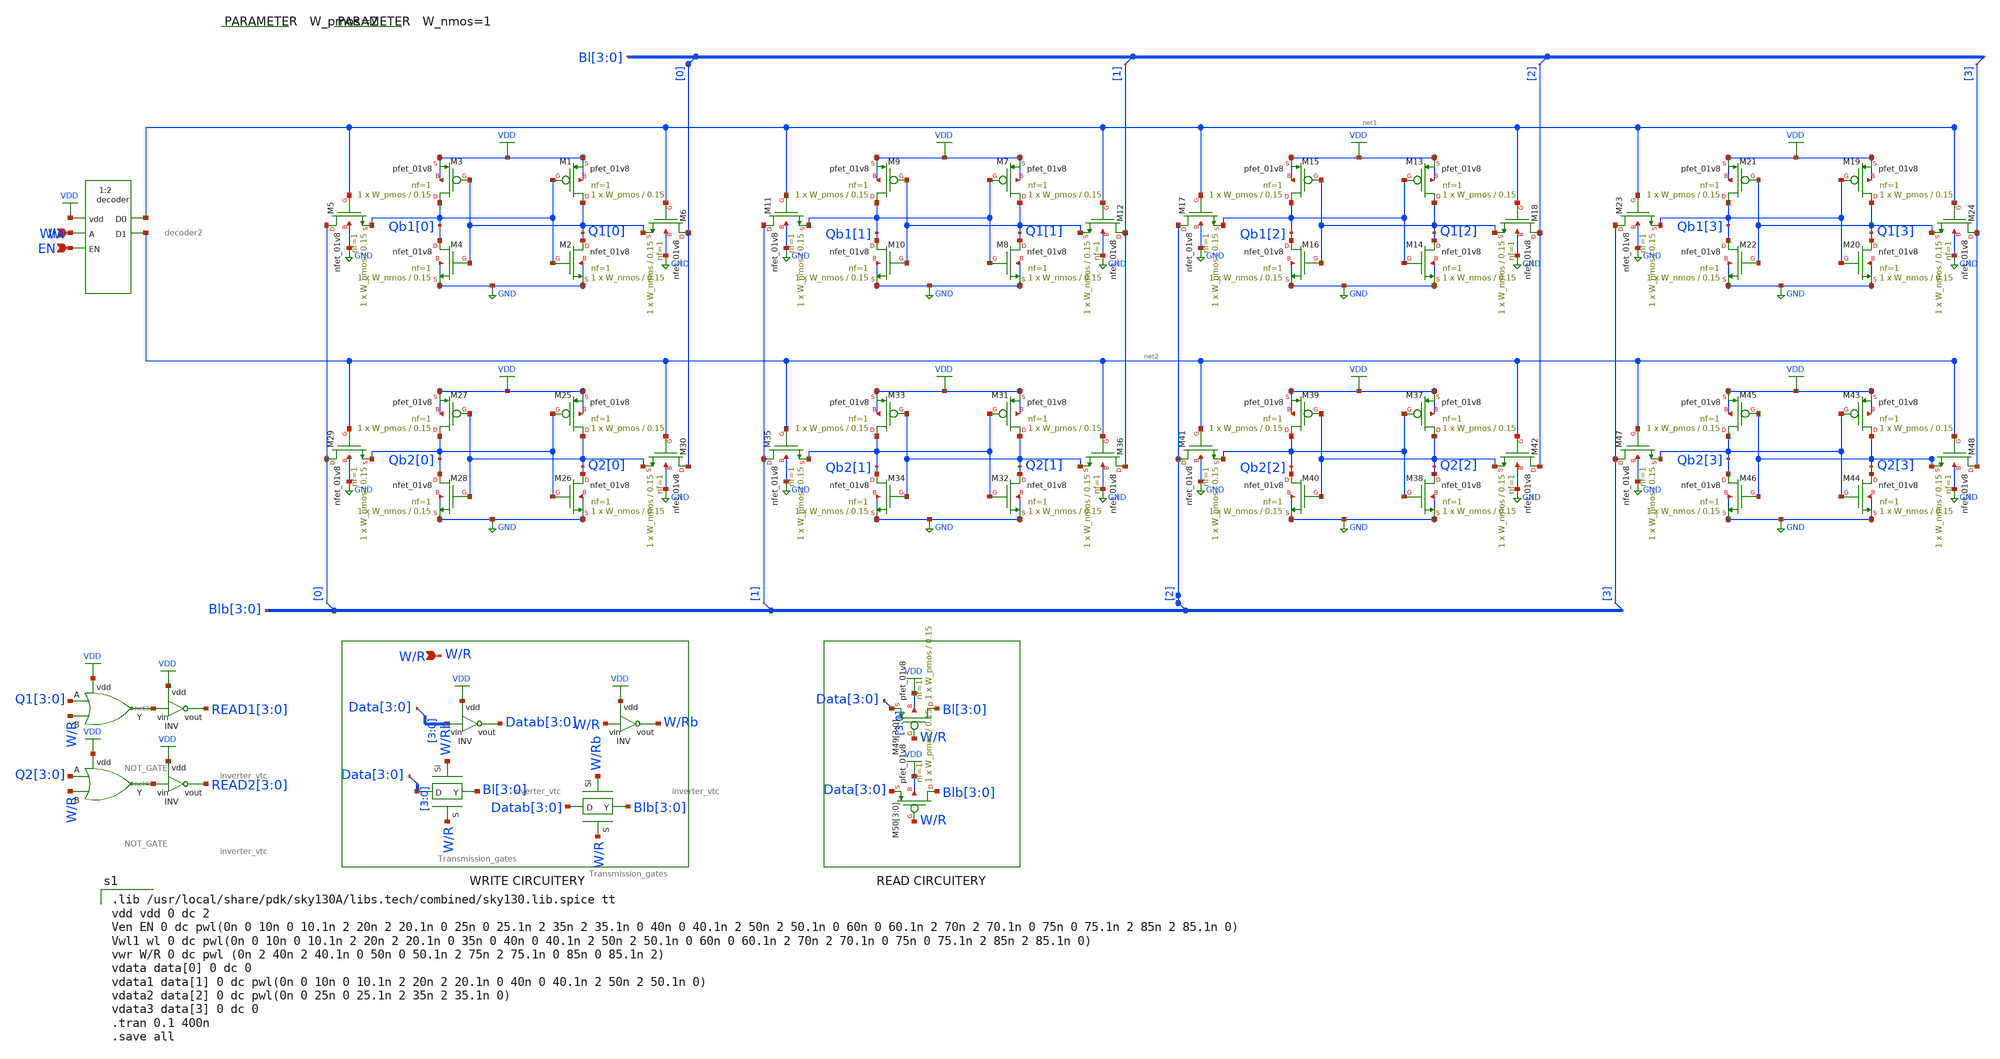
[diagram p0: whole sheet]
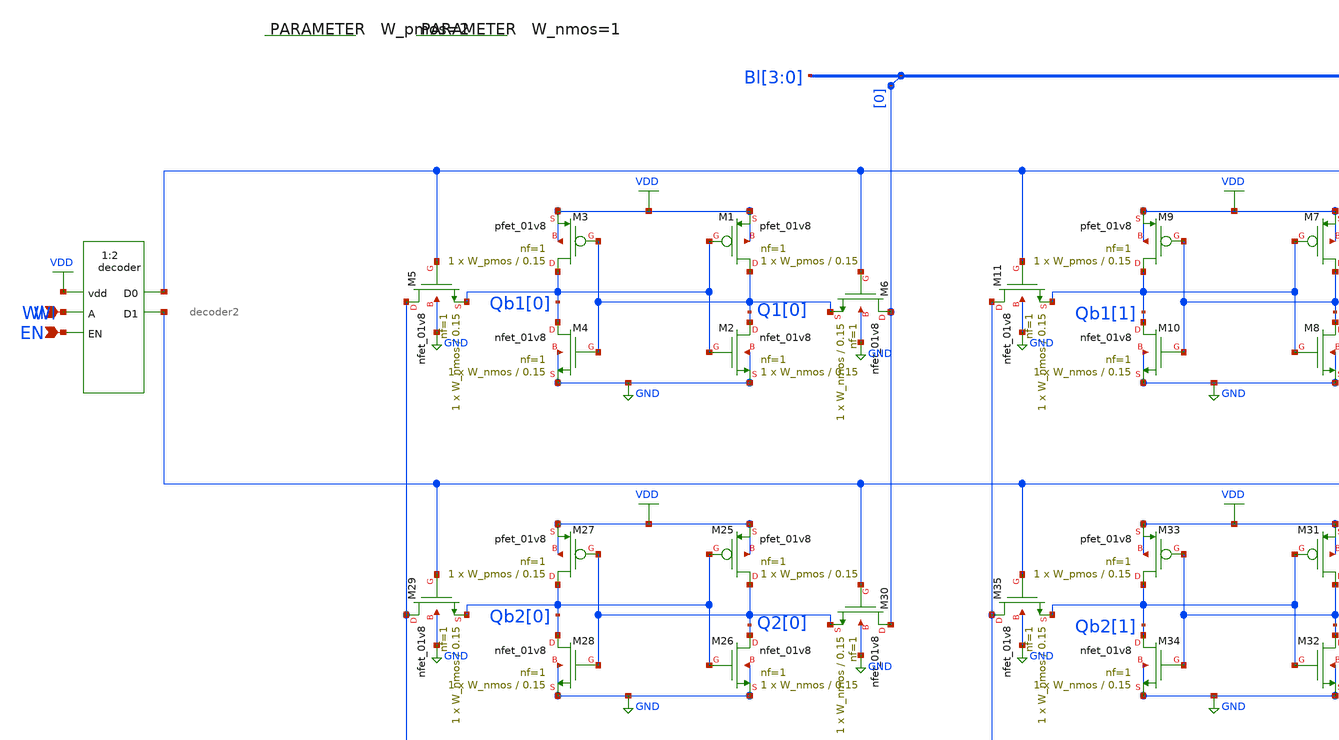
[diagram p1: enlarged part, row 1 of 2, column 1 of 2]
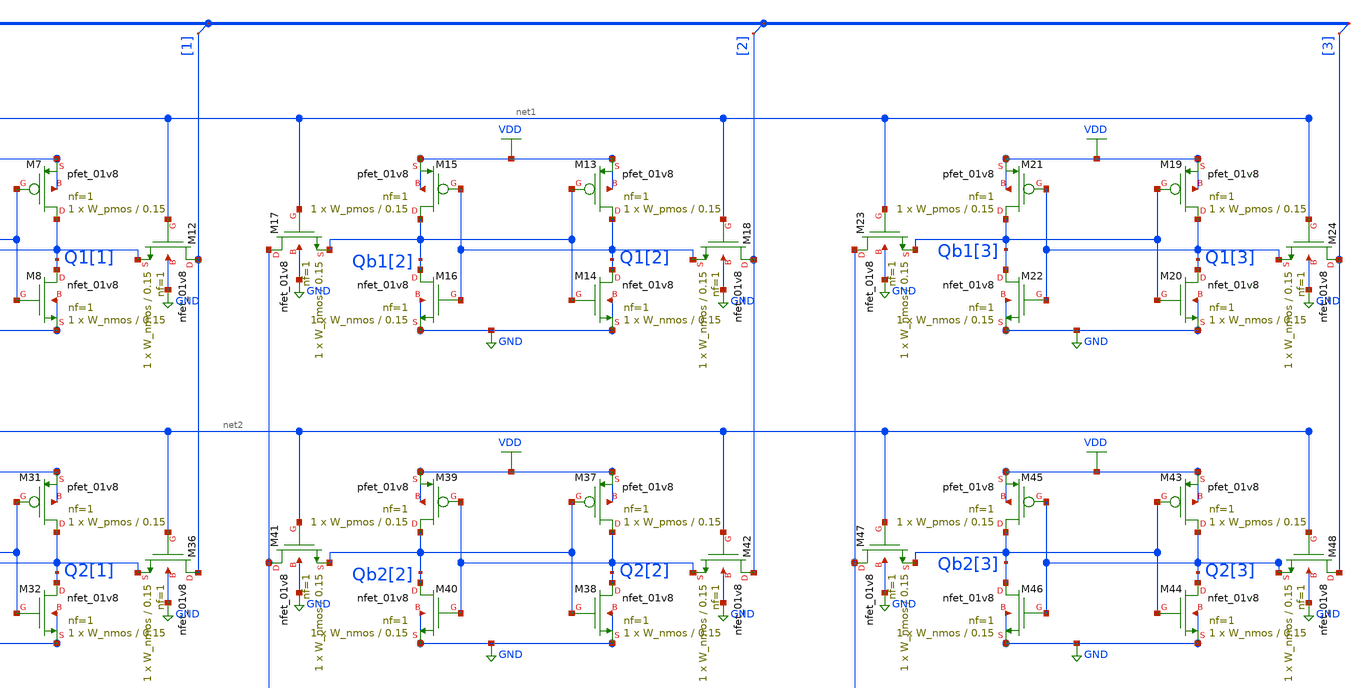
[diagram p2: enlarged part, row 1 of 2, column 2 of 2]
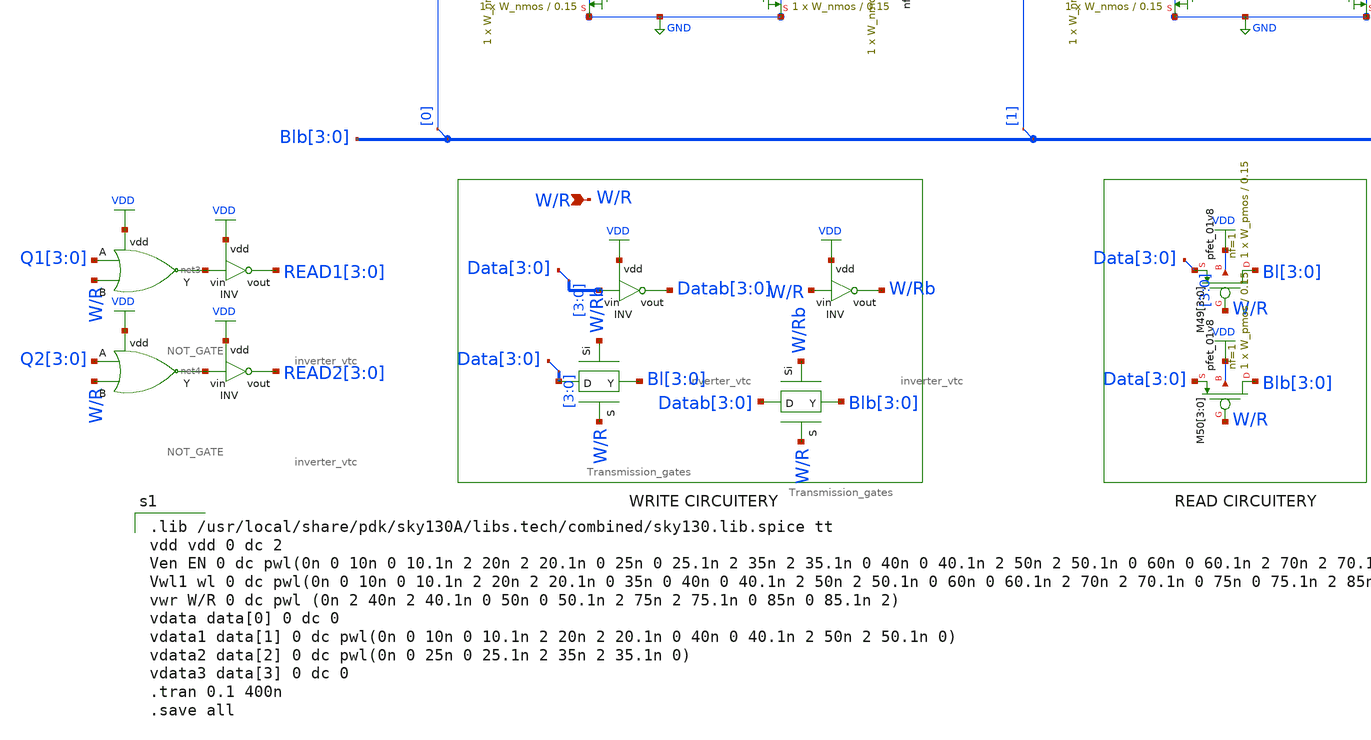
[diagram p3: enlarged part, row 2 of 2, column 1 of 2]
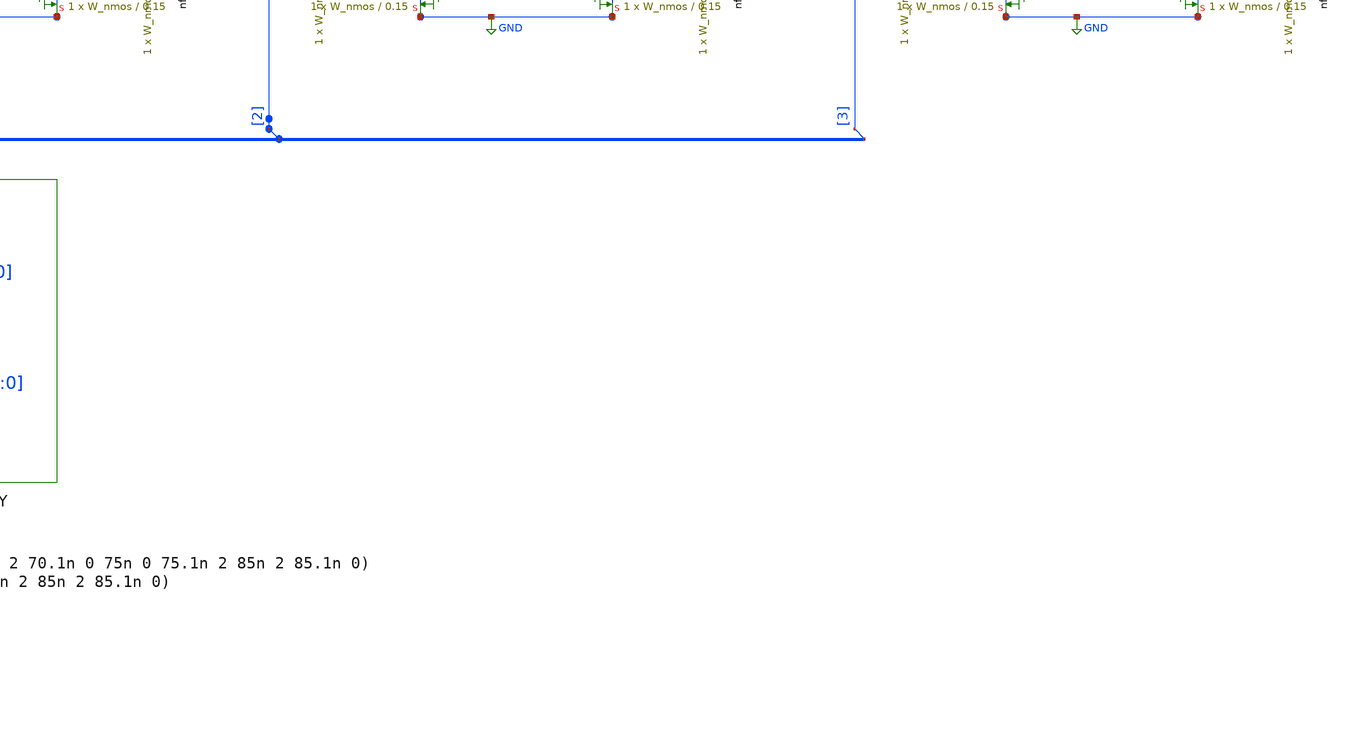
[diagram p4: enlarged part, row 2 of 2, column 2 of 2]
** sch_path: Circuit Files/circuits/circuits/8RAMF.sch
**.subckt 8RAMF Wl W/R EN
*.ipin Wl
*.ipin W/R
*.ipin EN
XM1 Q1[0] Qb1[0] VDD VDD sky130_fd_pr__pfet_01v8 L=0.15 W=W_pmos nf=1 ad='int((nf+1)/2) * W/nf * 0.29'
+ as='int((nf+2)/2) * W/nf * 0.29' pd='2*int((nf+1)/2) * (W/nf + 0.29)' ps='2*int((nf+2)/2) * (W/nf + 0.29)'
+ nrd='0.29 / W' nrs='0.29 / W' sa=0 sb=0 sd=0 mult=1 m=1
XM2 Q1[0] Qb1[0] GND GND sky130_fd_pr__nfet_01v8 L=0.15 W=W_nmos nf=1 ad='int((nf+1)/2) * W/nf * 0.29'
+ as='int((nf+2)/2) * W/nf * 0.29' pd='2*int((nf+1)/2) * (W/nf + 0.29)' ps='2*int((nf+2)/2) * (W/nf + 0.29)'
+ nrd='0.29 / W' nrs='0.29 / W' sa=0 sb=0 sd=0 mult=1 m=1
XM3 Qb1[0] Q1[0] VDD VDD sky130_fd_pr__pfet_01v8 L=0.15 W=W_pmos nf=1 ad='int((nf+1)/2) * W/nf * 0.29'
+ as='int((nf+2)/2) * W/nf * 0.29' pd='2*int((nf+1)/2) * (W/nf + 0.29)' ps='2*int((nf+2)/2) * (W/nf + 0.29)'
+ nrd='0.29 / W' nrs='0.29 / W' sa=0 sb=0 sd=0 mult=1 m=1
XM4 Qb1[0] Q1[0] GND GND sky130_fd_pr__nfet_01v8 L=0.15 W=W_nmos nf=1 ad='int((nf+1)/2) * W/nf * 0.29'
+ as='int((nf+2)/2) * W/nf * 0.29' pd='2*int((nf+1)/2) * (W/nf + 0.29)' ps='2*int((nf+2)/2) * (W/nf + 0.29)'
+ nrd='0.29 / W' nrs='0.29 / W' sa=0 sb=0 sd=0 mult=1 m=1
XM5 Blb[0] net1 Qb1[0] GND sky130_fd_pr__nfet_01v8 L=0.15 W=W_nmos nf=1 ad='int((nf+1)/2) * W/nf * 0.29'
+ as='int((nf+2)/2) * W/nf * 0.29' pd='2*int((nf+1)/2) * (W/nf + 0.29)' ps='2*int((nf+2)/2) * (W/nf + 0.29)'
+ nrd='0.29 / W' nrs='0.29 / W' sa=0 sb=0 sd=0 mult=1 m=1
XM6 Bl[0] net1 Q1[0] GND sky130_fd_pr__nfet_01v8 L=0.15 W=W_nmos nf=1 ad='int((nf+1)/2) * W/nf * 0.29'
+ as='int((nf+2)/2) * W/nf * 0.29' pd='2*int((nf+1)/2) * (W/nf + 0.29)' ps='2*int((nf+2)/2) * (W/nf + 0.29)'
+ nrd='0.29 / W' nrs='0.29 / W' sa=0 sb=0 sd=0 mult=1 m=1
XM7 Q1[1] Qb1[1] VDD VDD sky130_fd_pr__pfet_01v8 L=0.15 W=W_pmos nf=1 ad='int((nf+1)/2) * W/nf * 0.29'
+ as='int((nf+2)/2) * W/nf * 0.29' pd='2*int((nf+1)/2) * (W/nf + 0.29)' ps='2*int((nf+2)/2) * (W/nf + 0.29)'
+ nrd='0.29 / W' nrs='0.29 / W' sa=0 sb=0 sd=0 mult=1 m=1
XM8 Q1[1] Qb1[1] GND GND sky130_fd_pr__nfet_01v8 L=0.15 W=W_nmos nf=1 ad='int((nf+1)/2) * W/nf * 0.29'
+ as='int((nf+2)/2) * W/nf * 0.29' pd='2*int((nf+1)/2) * (W/nf + 0.29)' ps='2*int((nf+2)/2) * (W/nf + 0.29)'
+ nrd='0.29 / W' nrs='0.29 / W' sa=0 sb=0 sd=0 mult=1 m=1
XM9 Qb1[1] Q1[1] VDD VDD sky130_fd_pr__pfet_01v8 L=0.15 W=W_pmos nf=1 ad='int((nf+1)/2) * W/nf * 0.29'
+ as='int((nf+2)/2) * W/nf * 0.29' pd='2*int((nf+1)/2) * (W/nf + 0.29)' ps='2*int((nf+2)/2) * (W/nf + 0.29)'
+ nrd='0.29 / W' nrs='0.29 / W' sa=0 sb=0 sd=0 mult=1 m=1
XM10 Qb1[1] Q1[1] GND GND sky130_fd_pr__nfet_01v8 L=0.15 W=W_nmos nf=1 ad='int((nf+1)/2) * W/nf * 0.29'
+ as='int((nf+2)/2) * W/nf * 0.29' pd='2*int((nf+1)/2) * (W/nf + 0.29)' ps='2*int((nf+2)/2) * (W/nf + 0.29)'
+ nrd='0.29 / W' nrs='0.29 / W' sa=0 sb=0 sd=0 mult=1 m=1
XM11 Blb[1] net1 Qb1[1] GND sky130_fd_pr__nfet_01v8 L=0.15 W=W_nmos nf=1 ad='int((nf+1)/2) * W/nf * 0.29'
+ as='int((nf+2)/2) * W/nf * 0.29' pd='2*int((nf+1)/2) * (W/nf + 0.29)' ps='2*int((nf+2)/2) * (W/nf + 0.29)'
+ nrd='0.29 / W' nrs='0.29 / W' sa=0 sb=0 sd=0 mult=1 m=1
XM12 Bl[1] net1 Q1[1] GND sky130_fd_pr__nfet_01v8 L=0.15 W=W_nmos nf=1 ad='int((nf+1)/2) * W/nf * 0.29'
+ as='int((nf+2)/2) * W/nf * 0.29' pd='2*int((nf+1)/2) * (W/nf + 0.29)' ps='2*int((nf+2)/2) * (W/nf + 0.29)'
+ nrd='0.29 / W' nrs='0.29 / W' sa=0 sb=0 sd=0 mult=1 m=1
XM13 Q1[2] Qb1[2] VDD VDD sky130_fd_pr__pfet_01v8 L=0.15 W=W_pmos nf=1 ad='int((nf+1)/2) * W/nf * 0.29'
+ as='int((nf+2)/2) * W/nf * 0.29' pd='2*int((nf+1)/2) * (W/nf + 0.29)' ps='2*int((nf+2)/2) * (W/nf + 0.29)'
+ nrd='0.29 / W' nrs='0.29 / W' sa=0 sb=0 sd=0 mult=1 m=1
XM14 Q1[2] Qb1[2] GND GND sky130_fd_pr__nfet_01v8 L=0.15 W=W_nmos nf=1 ad='int((nf+1)/2) * W/nf * 0.29'
+ as='int((nf+2)/2) * W/nf * 0.29' pd='2*int((nf+1)/2) * (W/nf + 0.29)' ps='2*int((nf+2)/2) * (W/nf + 0.29)'
+ nrd='0.29 / W' nrs='0.29 / W' sa=0 sb=0 sd=0 mult=1 m=1
XM15 Qb1[2] Q1[2] VDD VDD sky130_fd_pr__pfet_01v8 L=0.15 W=W_pmos nf=1 ad='int((nf+1)/2) * W/nf * 0.29'
+ as='int((nf+2)/2) * W/nf * 0.29' pd='2*int((nf+1)/2) * (W/nf + 0.29)' ps='2*int((nf+2)/2) * (W/nf + 0.29)'
+ nrd='0.29 / W' nrs='0.29 / W' sa=0 sb=0 sd=0 mult=1 m=1
XM16 Qb1[2] Q1[2] GND GND sky130_fd_pr__nfet_01v8 L=0.15 W=W_nmos nf=1 ad='int((nf+1)/2) * W/nf * 0.29'
+ as='int((nf+2)/2) * W/nf * 0.29' pd='2*int((nf+1)/2) * (W/nf + 0.29)' ps='2*int((nf+2)/2) * (W/nf + 0.29)'
+ nrd='0.29 / W' nrs='0.29 / W' sa=0 sb=0 sd=0 mult=1 m=1
XM17 Blb[2] net1 Qb1[2] GND sky130_fd_pr__nfet_01v8 L=0.15 W=W_nmos nf=1 ad='int((nf+1)/2) * W/nf * 0.29'
+ as='int((nf+2)/2) * W/nf * 0.29' pd='2*int((nf+1)/2) * (W/nf + 0.29)' ps='2*int((nf+2)/2) * (W/nf + 0.29)'
+ nrd='0.29 / W' nrs='0.29 / W' sa=0 sb=0 sd=0 mult=1 m=1
XM18 Bl[2] net1 Q1[2] GND sky130_fd_pr__nfet_01v8 L=0.15 W=W_nmos nf=1 ad='int((nf+1)/2) * W/nf * 0.29'
+ as='int((nf+2)/2) * W/nf * 0.29' pd='2*int((nf+1)/2) * (W/nf + 0.29)' ps='2*int((nf+2)/2) * (W/nf + 0.29)'
+ nrd='0.29 / W' nrs='0.29 / W' sa=0 sb=0 sd=0 mult=1 m=1
XM19 Q1[3] Qb1[3] VDD VDD sky130_fd_pr__pfet_01v8 L=0.15 W=W_pmos nf=1 ad='int((nf+1)/2) * W/nf * 0.29'
+ as='int((nf+2)/2) * W/nf * 0.29' pd='2*int((nf+1)/2) * (W/nf + 0.29)' ps='2*int((nf+2)/2) * (W/nf + 0.29)'
+ nrd='0.29 / W' nrs='0.29 / W' sa=0 sb=0 sd=0 mult=1 m=1
XM20 Q1[3] Qb1[3] GND GND sky130_fd_pr__nfet_01v8 L=0.15 W=W_nmos nf=1 ad='int((nf+1)/2) * W/nf * 0.29'
+ as='int((nf+2)/2) * W/nf * 0.29' pd='2*int((nf+1)/2) * (W/nf + 0.29)' ps='2*int((nf+2)/2) * (W/nf + 0.29)'
+ nrd='0.29 / W' nrs='0.29 / W' sa=0 sb=0 sd=0 mult=1 m=1
XM21 Qb1[3] Q1[3] VDD VDD sky130_fd_pr__pfet_01v8 L=0.15 W=W_pmos nf=1 ad='int((nf+1)/2) * W/nf * 0.29'
+ as='int((nf+2)/2) * W/nf * 0.29' pd='2*int((nf+1)/2) * (W/nf + 0.29)' ps='2*int((nf+2)/2) * (W/nf + 0.29)'
+ nrd='0.29 / W' nrs='0.29 / W' sa=0 sb=0 sd=0 mult=1 m=1
XM22 Qb1[3] Q1[3] GND GND sky130_fd_pr__nfet_01v8 L=0.15 W=W_nmos nf=1 ad='int((nf+1)/2) * W/nf * 0.29'
+ as='int((nf+2)/2) * W/nf * 0.29' pd='2*int((nf+1)/2) * (W/nf + 0.29)' ps='2*int((nf+2)/2) * (W/nf + 0.29)'
+ nrd='0.29 / W' nrs='0.29 / W' sa=0 sb=0 sd=0 mult=1 m=1
XM23 Blb[3] net1 Qb1[3] GND sky130_fd_pr__nfet_01v8 L=0.15 W=W_nmos nf=1 ad='int((nf+1)/2) * W/nf * 0.29'
+ as='int((nf+2)/2) * W/nf * 0.29' pd='2*int((nf+1)/2) * (W/nf + 0.29)' ps='2*int((nf+2)/2) * (W/nf + 0.29)'
+ nrd='0.29 / W' nrs='0.29 / W' sa=0 sb=0 sd=0 mult=1 m=1
XM24 Bl[3] net1 Q1[3] GND sky130_fd_pr__nfet_01v8 L=0.15 W=W_nmos nf=1 ad='int((nf+1)/2) * W/nf * 0.29'
+ as='int((nf+2)/2) * W/nf * 0.29' pd='2*int((nf+1)/2) * (W/nf + 0.29)' ps='2*int((nf+2)/2) * (W/nf + 0.29)'
+ nrd='0.29 / W' nrs='0.29 / W' sa=0 sb=0 sd=0 mult=1 m=1
XM25 Q2[0] Qb2[0] VDD VDD sky130_fd_pr__pfet_01v8 L=0.15 W=W_pmos nf=1 ad='int((nf+1)/2) * W/nf * 0.29'
+ as='int((nf+2)/2) * W/nf * 0.29' pd='2*int((nf+1)/2) * (W/nf + 0.29)' ps='2*int((nf+2)/2) * (W/nf + 0.29)'
+ nrd='0.29 / W' nrs='0.29 / W' sa=0 sb=0 sd=0 mult=1 m=1
XM26 Q2[0] Qb2[0] GND GND sky130_fd_pr__nfet_01v8 L=0.15 W=W_nmos nf=1 ad='int((nf+1)/2) * W/nf * 0.29'
+ as='int((nf+2)/2) * W/nf * 0.29' pd='2*int((nf+1)/2) * (W/nf + 0.29)' ps='2*int((nf+2)/2) * (W/nf + 0.29)'
+ nrd='0.29 / W' nrs='0.29 / W' sa=0 sb=0 sd=0 mult=1 m=1
XM27 Qb2[0] Q2[0] VDD VDD sky130_fd_pr__pfet_01v8 L=0.15 W=W_pmos nf=1 ad='int((nf+1)/2) * W/nf * 0.29'
+ as='int((nf+2)/2) * W/nf * 0.29' pd='2*int((nf+1)/2) * (W/nf + 0.29)' ps='2*int((nf+2)/2) * (W/nf + 0.29)'
+ nrd='0.29 / W' nrs='0.29 / W' sa=0 sb=0 sd=0 mult=1 m=1
XM28 Qb2[0] Q2[0] GND GND sky130_fd_pr__nfet_01v8 L=0.15 W=W_nmos nf=1 ad='int((nf+1)/2) * W/nf * 0.29'
+ as='int((nf+2)/2) * W/nf * 0.29' pd='2*int((nf+1)/2) * (W/nf + 0.29)' ps='2*int((nf+2)/2) * (W/nf + 0.29)'
+ nrd='0.29 / W' nrs='0.29 / W' sa=0 sb=0 sd=0 mult=1 m=1
XM29 Blb[0] net2 Qb2[0] GND sky130_fd_pr__nfet_01v8 L=0.15 W=W_nmos nf=1 ad='int((nf+1)/2) * W/nf * 0.29'
+ as='int((nf+2)/2) * W/nf * 0.29' pd='2*int((nf+1)/2) * (W/nf + 0.29)' ps='2*int((nf+2)/2) * (W/nf + 0.29)'
+ nrd='0.29 / W' nrs='0.29 / W' sa=0 sb=0 sd=0 mult=1 m=1
XM30 Bl[0] net2 Q2[0] GND sky130_fd_pr__nfet_01v8 L=0.15 W=W_nmos nf=1 ad='int((nf+1)/2) * W/nf * 0.29'
+ as='int((nf+2)/2) * W/nf * 0.29' pd='2*int((nf+1)/2) * (W/nf + 0.29)' ps='2*int((nf+2)/2) * (W/nf + 0.29)'
+ nrd='0.29 / W' nrs='0.29 / W' sa=0 sb=0 sd=0 mult=1 m=1
XM31 Q2[1] Qb2[1] VDD VDD sky130_fd_pr__pfet_01v8 L=0.15 W=W_pmos nf=1 ad='int((nf+1)/2) * W/nf * 0.29'
+ as='int((nf+2)/2) * W/nf * 0.29' pd='2*int((nf+1)/2) * (W/nf + 0.29)' ps='2*int((nf+2)/2) * (W/nf + 0.29)'
+ nrd='0.29 / W' nrs='0.29 / W' sa=0 sb=0 sd=0 mult=1 m=1
XM32 Q2[1] Qb2[1] GND GND sky130_fd_pr__nfet_01v8 L=0.15 W=W_nmos nf=1 ad='int((nf+1)/2) * W/nf * 0.29'
+ as='int((nf+2)/2) * W/nf * 0.29' pd='2*int((nf+1)/2) * (W/nf + 0.29)' ps='2*int((nf+2)/2) * (W/nf + 0.29)'
+ nrd='0.29 / W' nrs='0.29 / W' sa=0 sb=0 sd=0 mult=1 m=1
XM33 Qb2[1] Q2[1] VDD VDD sky130_fd_pr__pfet_01v8 L=0.15 W=W_pmos nf=1 ad='int((nf+1)/2) * W/nf * 0.29'
+ as='int((nf+2)/2) * W/nf * 0.29' pd='2*int((nf+1)/2) * (W/nf + 0.29)' ps='2*int((nf+2)/2) * (W/nf + 0.29)'
+ nrd='0.29 / W' nrs='0.29 / W' sa=0 sb=0 sd=0 mult=1 m=1
XM34 Qb2[1] Q2[1] GND GND sky130_fd_pr__nfet_01v8 L=0.15 W=W_nmos nf=1 ad='int((nf+1)/2) * W/nf * 0.29'
+ as='int((nf+2)/2) * W/nf * 0.29' pd='2*int((nf+1)/2) * (W/nf + 0.29)' ps='2*int((nf+2)/2) * (W/nf + 0.29)'
+ nrd='0.29 / W' nrs='0.29 / W' sa=0 sb=0 sd=0 mult=1 m=1
XM35 Blb[1] net2 Qb2[1] GND sky130_fd_pr__nfet_01v8 L=0.15 W=W_nmos nf=1 ad='int((nf+1)/2) * W/nf * 0.29'
+ as='int((nf+2)/2) * W/nf * 0.29' pd='2*int((nf+1)/2) * (W/nf + 0.29)' ps='2*int((nf+2)/2) * (W/nf + 0.29)'
+ nrd='0.29 / W' nrs='0.29 / W' sa=0 sb=0 sd=0 mult=1 m=1
XM36 Bl[1] net2 Q2[1] GND sky130_fd_pr__nfet_01v8 L=0.15 W=W_nmos nf=1 ad='int((nf+1)/2) * W/nf * 0.29'
+ as='int((nf+2)/2) * W/nf * 0.29' pd='2*int((nf+1)/2) * (W/nf + 0.29)' ps='2*int((nf+2)/2) * (W/nf + 0.29)'
+ nrd='0.29 / W' nrs='0.29 / W' sa=0 sb=0 sd=0 mult=1 m=1
XM37 Q2[2] Qb2[2] VDD VDD sky130_fd_pr__pfet_01v8 L=0.15 W=W_pmos nf=1 ad='int((nf+1)/2) * W/nf * 0.29'
+ as='int((nf+2)/2) * W/nf * 0.29' pd='2*int((nf+1)/2) * (W/nf + 0.29)' ps='2*int((nf+2)/2) * (W/nf + 0.29)'
+ nrd='0.29 / W' nrs='0.29 / W' sa=0 sb=0 sd=0 mult=1 m=1
XM38 Q2[2] Qb2[2] GND GND sky130_fd_pr__nfet_01v8 L=0.15 W=W_nmos nf=1 ad='int((nf+1)/2) * W/nf * 0.29'
+ as='int((nf+2)/2) * W/nf * 0.29' pd='2*int((nf+1)/2) * (W/nf + 0.29)' ps='2*int((nf+2)/2) * (W/nf + 0.29)'
+ nrd='0.29 / W' nrs='0.29 / W' sa=0 sb=0 sd=0 mult=1 m=1
XM39 Qb2[2] Q2[2] VDD VDD sky130_fd_pr__pfet_01v8 L=0.15 W=W_pmos nf=1 ad='int((nf+1)/2) * W/nf * 0.29'
+ as='int((nf+2)/2) * W/nf * 0.29' pd='2*int((nf+1)/2) * (W/nf + 0.29)' ps='2*int((nf+2)/2) * (W/nf + 0.29)'
+ nrd='0.29 / W' nrs='0.29 / W' sa=0 sb=0 sd=0 mult=1 m=1
XM40 Qb2[2] Q2[2] GND GND sky130_fd_pr__nfet_01v8 L=0.15 W=W_nmos nf=1 ad='int((nf+1)/2) * W/nf * 0.29'
+ as='int((nf+2)/2) * W/nf * 0.29' pd='2*int((nf+1)/2) * (W/nf + 0.29)' ps='2*int((nf+2)/2) * (W/nf + 0.29)'
+ nrd='0.29 / W' nrs='0.29 / W' sa=0 sb=0 sd=0 mult=1 m=1
XM41 Blb[2] net2 Qb2[2] GND sky130_fd_pr__nfet_01v8 L=0.15 W=W_nmos nf=1 ad='int((nf+1)/2) * W/nf * 0.29'
+ as='int((nf+2)/2) * W/nf * 0.29' pd='2*int((nf+1)/2) * (W/nf + 0.29)' ps='2*int((nf+2)/2) * (W/nf + 0.29)'
+ nrd='0.29 / W' nrs='0.29 / W' sa=0 sb=0 sd=0 mult=1 m=1
XM42 Bl[2] net2 Q2[2] GND sky130_fd_pr__nfet_01v8 L=0.15 W=W_nmos nf=1 ad='int((nf+1)/2) * W/nf * 0.29'
+ as='int((nf+2)/2) * W/nf * 0.29' pd='2*int((nf+1)/2) * (W/nf + 0.29)' ps='2*int((nf+2)/2) * (W/nf + 0.29)'
+ nrd='0.29 / W' nrs='0.29 / W' sa=0 sb=0 sd=0 mult=1 m=1
XM43 Q2[3] Qb2[3] VDD VDD sky130_fd_pr__pfet_01v8 L=0.15 W=W_pmos nf=1 ad='int((nf+1)/2) * W/nf * 0.29'
+ as='int((nf+2)/2) * W/nf * 0.29' pd='2*int((nf+1)/2) * (W/nf + 0.29)' ps='2*int((nf+2)/2) * (W/nf + 0.29)'
+ nrd='0.29 / W' nrs='0.29 / W' sa=0 sb=0 sd=0 mult=1 m=1
XM44 Q2[3] Qb2[3] GND GND sky130_fd_pr__nfet_01v8 L=0.15 W=W_nmos nf=1 ad='int((nf+1)/2) * W/nf * 0.29'
+ as='int((nf+2)/2) * W/nf * 0.29' pd='2*int((nf+1)/2) * (W/nf + 0.29)' ps='2*int((nf+2)/2) * (W/nf + 0.29)'
+ nrd='0.29 / W' nrs='0.29 / W' sa=0 sb=0 sd=0 mult=1 m=1
XM45 Qb2[3] Q2[3] VDD VDD sky130_fd_pr__pfet_01v8 L=0.15 W=W_pmos nf=1 ad='int((nf+1)/2) * W/nf * 0.29'
+ as='int((nf+2)/2) * W/nf * 0.29' pd='2*int((nf+1)/2) * (W/nf + 0.29)' ps='2*int((nf+2)/2) * (W/nf + 0.29)'
+ nrd='0.29 / W' nrs='0.29 / W' sa=0 sb=0 sd=0 mult=1 m=1
XM46 Qb2[3] Q2[3] GND GND sky130_fd_pr__nfet_01v8 L=0.15 W=W_nmos nf=1 ad='int((nf+1)/2) * W/nf * 0.29'
+ as='int((nf+2)/2) * W/nf * 0.29' pd='2*int((nf+1)/2) * (W/nf + 0.29)' ps='2*int((nf+2)/2) * (W/nf + 0.29)'
+ nrd='0.29 / W' nrs='0.29 / W' sa=0 sb=0 sd=0 mult=1 m=1
XM47 Blb[3] net2 Qb2[3] GND sky130_fd_pr__nfet_01v8 L=0.15 W=W_nmos nf=1 ad='int((nf+1)/2) * W/nf * 0.29'
+ as='int((nf+2)/2) * W/nf * 0.29' pd='2*int((nf+1)/2) * (W/nf + 0.29)' ps='2*int((nf+2)/2) * (W/nf + 0.29)'
+ nrd='0.29 / W' nrs='0.29 / W' sa=0 sb=0 sd=0 mult=1 m=1
XM48 Bl[3] net2 Q2[3] GND sky130_fd_pr__nfet_01v8 L=0.15 W=W_nmos nf=1 ad='int((nf+1)/2) * W/nf * 0.29'
+ as='int((nf+2)/2) * W/nf * 0.29' pd='2*int((nf+1)/2) * (W/nf + 0.29)' ps='2*int((nf+2)/2) * (W/nf + 0.29)'
+ nrd='0.29 / W' nrs='0.29 / W' sa=0 sb=0 sd=0 mult=1 m=1
* tap: Bl[3:0] --> Bl[0]
* tap: Bl[3:0] --> Bl[1]
* tap: Bl[3:0] --> Bl[2]
* tap: Bl[3:0] --> Bl[3]
* tap: Blb[3:0] --> Blb[0]
* tap: Blb[3:0] --> Blb[1]
* tap: Blb[3:0] --> Blb[2]
* tap: Blb[3:0] --> Blb[3]
x1 VDD net1 Wl net2 EN decoder2
x2[3] VDD Data[3] Datab[3] inverter_vtc
x2[2] VDD Data[2] Datab[2] inverter_vtc
x2[1] VDD Data[1] Datab[1] inverter_vtc
x2[0] VDD Data[0] Datab[0] inverter_vtc
x1[3] W/Rb Data[3] Bl[3] W/R Transmission_gates
x1[2] W/Rb Data[2] Bl[2] W/R Transmission_gates
x1[1] W/Rb Data[1] Bl[1] W/R Transmission_gates
x1[0] W/Rb Data[0] Bl[0] W/R Transmission_gates
x3 VDD W/R W/Rb inverter_vtc
* tap: Data[3:0] --> Data[3:0]
* tap: Data[3:0] --> Data[3:0]
* tap: Data[3:0] --> Data[3:0]
XM49[3] Bl[3] W/R Data[3] VDD sky130_fd_pr__pfet_01v8 L=0.15 W=W_pmos nf=1 ad='int((nf+1)/2) * W/nf * 0.29'
+ as='int((nf+2)/2) * W/nf * 0.29' pd='2*int((nf+1)/2) * (W/nf + 0.29)' ps='2*int((nf+2)/2) * (W/nf + 0.29)'
+ nrd='0.29 / W' nrs='0.29 / W' sa=0 sb=0 sd=0 mult=1 m=1
XM49[2] Bl[2] W/R Data[2] VDD sky130_fd_pr__pfet_01v8 L=0.15 W=W_pmos nf=1 ad='int((nf+1)/2) * W/nf * 0.29'
+ as='int((nf+2)/2) * W/nf * 0.29' pd='2*int((nf+1)/2) * (W/nf + 0.29)' ps='2*int((nf+2)/2) * (W/nf + 0.29)'
+ nrd='0.29 / W' nrs='0.29 / W' sa=0 sb=0 sd=0 mult=1 m=1
XM49[1] Bl[1] W/R Data[1] VDD sky130_fd_pr__pfet_01v8 L=0.15 W=W_pmos nf=1 ad='int((nf+1)/2) * W/nf * 0.29'
+ as='int((nf+2)/2) * W/nf * 0.29' pd='2*int((nf+1)/2) * (W/nf + 0.29)' ps='2*int((nf+2)/2) * (W/nf + 0.29)'
+ nrd='0.29 / W' nrs='0.29 / W' sa=0 sb=0 sd=0 mult=1 m=1
XM49[0] Bl[0] W/R Data[0] VDD sky130_fd_pr__pfet_01v8 L=0.15 W=W_pmos nf=1 ad='int((nf+1)/2) * W/nf * 0.29'
+ as='int((nf+2)/2) * W/nf * 0.29' pd='2*int((nf+1)/2) * (W/nf + 0.29)' ps='2*int((nf+2)/2) * (W/nf + 0.29)'
+ nrd='0.29 / W' nrs='0.29 / W' sa=0 sb=0 sd=0 mult=1 m=1
XM50[3] Blb[3] W/R Data[3] VDD sky130_fd_pr__pfet_01v8 L=0.15 W=W_pmos nf=1 ad='int((nf+1)/2) * W/nf * 0.29'
+ as='int((nf+2)/2) * W/nf * 0.29' pd='2*int((nf+1)/2) * (W/nf + 0.29)' ps='2*int((nf+2)/2) * (W/nf + 0.29)'
+ nrd='0.29 / W' nrs='0.29 / W' sa=0 sb=0 sd=0 mult=1 m=1
XM50[2] Blb[2] W/R Data[2] VDD sky130_fd_pr__pfet_01v8 L=0.15 W=W_pmos nf=1 ad='int((nf+1)/2) * W/nf * 0.29'
+ as='int((nf+2)/2) * W/nf * 0.29' pd='2*int((nf+1)/2) * (W/nf + 0.29)' ps='2*int((nf+2)/2) * (W/nf + 0.29)'
+ nrd='0.29 / W' nrs='0.29 / W' sa=0 sb=0 sd=0 mult=1 m=1
XM50[1] Blb[1] W/R Data[1] VDD sky130_fd_pr__pfet_01v8 L=0.15 W=W_pmos nf=1 ad='int((nf+1)/2) * W/nf * 0.29'
+ as='int((nf+2)/2) * W/nf * 0.29' pd='2*int((nf+1)/2) * (W/nf + 0.29)' ps='2*int((nf+2)/2) * (W/nf + 0.29)'
+ nrd='0.29 / W' nrs='0.29 / W' sa=0 sb=0 sd=0 mult=1 m=1
XM50[0] Blb[0] W/R Data[0] VDD sky130_fd_pr__pfet_01v8 L=0.15 W=W_pmos nf=1 ad='int((nf+1)/2) * W/nf * 0.29'
+ as='int((nf+2)/2) * W/nf * 0.29' pd='2*int((nf+1)/2) * (W/nf + 0.29)' ps='2*int((nf+2)/2) * (W/nf + 0.29)'
+ nrd='0.29 / W' nrs='0.29 / W' sa=0 sb=0 sd=0 mult=1 m=1
x3[3] W/Rb Datab[3] Blb[3] W/R Transmission_gates
x3[2] W/Rb Datab[2] Blb[2] W/R Transmission_gates
x3[1] W/Rb Datab[1] Blb[1] W/R Transmission_gates
x3[0] W/Rb Datab[0] Blb[0] W/R Transmission_gates
x4[3] VDD Q1[3] W/R net3[3] NOT_GATE
x4[2] VDD Q1[2] W/R net3[2] NOT_GATE
x4[1] VDD Q1[1] W/R net3[1] NOT_GATE
x4[0] VDD Q1[0] W/R net3[0] NOT_GATE
x5[3] VDD Q2[3] W/R net4[3] NOT_GATE
x5[2] VDD Q2[2] W/R net4[2] NOT_GATE
x5[1] VDD Q2[1] W/R net4[1] NOT_GATE
x5[0] VDD Q2[0] W/R net4[0] NOT_GATE
x7[3] VDD net4[3] READ2[3] inverter_vtc
x7[2] VDD net4[2] READ2[2] inverter_vtc
x7[1] VDD net4[1] READ2[1] inverter_vtc
x7[0] VDD net4[0] READ2[0] inverter_vtc
x6[3] VDD net3[3] READ1[3] inverter_vtc
x6[2] VDD net3[2] READ1[2] inverter_vtc
x6[1] VDD net3[1] READ1[1] inverter_vtc
x6[0] VDD net3[0] READ1[0] inverter_vtc
.param W_pmos=2
.param W_nmos=1
**** begin user architecture code

.lib /usr/local/share/pdk/sky130A/libs.tech/combined/sky130.lib.spice tt
vdd vdd 0 dc 2
Ven EN 0 dc pwl(0n 0 10n 0 10.1n 2 20n 2 20.1n 0 25n 0 25.1n 2 35n 2 35.1n 0 40n 0 40.1n 2 50n 2
+ 50.1n 0 60n 0 60.1n 2 70n 2 70.1n 0 75n 0 75.1n 2 85n 2 85.1n 0)
Vwl1 wl 0 dc pwl(0n 0 10n 0 10.1n 2 20n 2 20.1n 0 35n 0 40n 0 40.1n 2 50n 2 50.1n 0 60n 0 60.1n 2
+ 70n 2 70.1n 0 75n 0 75.1n 2 85n 2 85.1n 0)
vwr W/R 0 dc pwl (0n 2 40n 2 40.1n 0 50n 0 50.1n 2 75n 2 75.1n 0 85n 0 85.1n 2)
vdata data[0] 0 dc 0
vdata1 data[1] 0 dc pwl(0n 0 10n 0 10.1n 2 20n 2 20.1n 0 40n 0 40.1n 2 50n 2 50.1n 0)
vdata2 data[2] 0 dc pwl(0n 0 25n 0 25.1n 2 35n 2 35.1n 0)
vdata3 data[3] 0 dc 0
.tran 0.1 400n
.save all


**** end user architecture code
**.ends

* expanding   symbol:  daVLSI_World/circuits/decoder2.sym # of pins=5
** sym_path: Circuit Files/circuits/circuits/decoder2.sym
** sch_path: Circuit Files/circuits/circuits/decoder2.sch
.subckt decoder2 vdd D0 A D1 EN
*.ipin A
*.opin D0
*.opin D1
*.ipin vdd
*.ipin EN
x1 vdd Ab D0 EN AND_gate
x2 vdd A D1 EN AND_gate
x3 vdd A Ab inverter_vtc
.ends


* expanding   symbol:  daVLSI_World/gates/inverter_vtc.sym # of pins=3
** sym_path: Circuit Files/Logic gate design using MOSFETS/gates/inverter_vtc.sym
** sch_path: Circuit Files/Logic gate design using MOSFETS/gates/inverter_vtc.sch
.subckt inverter_vtc vdd vin vout
*.ipin vin
*.opin vout
*.ipin vdd
XM1 vout vin GND GND sky130_fd_pr__nfet_01v8 L=0.15 W=1 nf=1 ad='int((nf+1)/2) * W/nf * 0.29' as='int((nf+2)/2) * W/nf * 0.29'
+ pd='2*int((nf+1)/2) * (W/nf + 0.29)' ps='2*int((nf+2)/2) * (W/nf + 0.29)' nrd='0.29 / W' nrs='0.29 / W'
+ sa=0 sb=0 sd=0 mult=1 m=1
XM2 vout vin vdd vdd sky130_fd_pr__pfet_01v8 L=0.15 W=2 nf=1 ad='int((nf+1)/2) * W/nf * 0.29' as='int((nf+2)/2) * W/nf * 0.29'
+ pd='2*int((nf+1)/2) * (W/nf + 0.29)' ps='2*int((nf+2)/2) * (W/nf + 0.29)' nrd='0.29 / W' nrs='0.29 / W'
+ sa=0 sb=0 sd=0 mult=1 m=1
.ends


* expanding   symbol:  daVLSI_World/first_test/Transmission_gates.sym # of pins=4
** sym_path: Circuit Files/circuits/circuits/Transmission_gates.sym
** sch_path: Circuit Files/circuits/circuits/Transmission_gates.sch
.subckt Transmission_gates Si D Y S
*.ipin D
*.opin Y
*.ipin Si
*.ipin S
XM1 D S Y GND sky130_fd_pr__nfet_01v8 L=0.15 W=1 nf=1 ad='int((nf+1)/2) * W/nf * 0.29' as='int((nf+2)/2) * W/nf * 0.29'
+ pd='2*int((nf+1)/2) * (W/nf + 0.29)' ps='2*int((nf+2)/2) * (W/nf + 0.29)' nrd='0.29 / W' nrs='0.29 / W'
+ sa=0 sb=0 sd=0 mult=1 m=1
XM4 D Si Y net1 sky130_fd_pr__pfet_01v8 L=0.15 W=2 nf=1 ad='int((nf+1)/2) * W/nf * 0.29' as='int((nf+2)/2) * W/nf * 0.29'
+ pd='2*int((nf+1)/2) * (W/nf + 0.29)' ps='2*int((nf+2)/2) * (W/nf + 0.29)' nrd='0.29 / W' nrs='0.29 / W'
+ sa=0 sb=0 sd=0 mult=1 m=1
Vdd net1 GND 1.8
.ends


* expanding   symbol:  daVLSI_World/gates/NOT_GATE.sym # of pins=4
** sym_path: Circuit Files/Logic gate design using MOSFETS/gates/NOT_GATE.sym
** sch_path: Circuit Files/Logic gate design using MOSFETS/gates/NOT_GATE.sch
.subckt NOT_GATE vdd A B Y
*.ipin A
*.ipin B
*.ipin vdd
*.opin Y
XM1 Y B net1 vdd sky130_fd_pr__pfet_01v8 L=0.15 W=2 nf=1 ad='int((nf+1)/2) * W/nf * 0.29' as='int((nf+2)/2) * W/nf * 0.29'
+ pd='2*int((nf+1)/2) * (W/nf + 0.29)' ps='2*int((nf+2)/2) * (W/nf + 0.29)' nrd='0.29 / W' nrs='0.29 / W'
+ sa=0 sb=0 sd=0 mult=1 m=1
XM2 net1 A vdd vdd sky130_fd_pr__pfet_01v8 L=0.15 W=2 nf=1 ad='int((nf+1)/2) * W/nf * 0.29' as='int((nf+2)/2) * W/nf * 0.29'
+ pd='2*int((nf+1)/2) * (W/nf + 0.29)' ps='2*int((nf+2)/2) * (W/nf + 0.29)' nrd='0.29 / W' nrs='0.29 / W'
+ sa=0 sb=0 sd=0 mult=1 m=1
XM3 Y B GND GND sky130_fd_pr__nfet_01v8 L=0.15 W=1 nf=1 ad='int((nf+1)/2) * W/nf * 0.29' as='int((nf+2)/2) * W/nf * 0.29'
+ pd='2*int((nf+1)/2) * (W/nf + 0.29)' ps='2*int((nf+2)/2) * (W/nf + 0.29)' nrd='0.29 / W' nrs='0.29 / W'
+ sa=0 sb=0 sd=0 mult=1 m=1
XM4 Y A GND GND sky130_fd_pr__nfet_01v8 L=0.15 W=1 nf=1 ad='int((nf+1)/2) * W/nf * 0.29' as='int((nf+2)/2) * W/nf * 0.29'
+ pd='2*int((nf+1)/2) * (W/nf + 0.29)' ps='2*int((nf+2)/2) * (W/nf + 0.29)' nrd='0.29 / W' nrs='0.29 / W'
+ sa=0 sb=0 sd=0 mult=1 m=1
.ends


* expanding   symbol:  daVLSI_World/gates/AND_gate.sym # of pins=4
** sym_path: Circuit Files/Logic gate design using MOSFETS/gates/AND_gate.sym
** sch_path: Circuit Files/Logic gate design using MOSFETS/gates/AND_gate.sch
.subckt AND_gate vdd A Y B
*.opin Y
*.ipin A
*.ipin B
*.ipin vdd
x1 vdd net1 A B GND NAND_gate
x2 vdd net1 Y inverter_vtc
.ends


* expanding   symbol:  daVLSI_World/gates/NAND_gate.sym # of pins=5
** sym_path: Circuit Files/Logic gate design using MOSFETS/gates/NAND_gate.sym
** sch_path: Circuit Files/Logic gate design using MOSFETS/gates/NAND_gate.sch
.subckt NAND_gate vdd Y A B gnd
*.ipin A
*.ipin B
*.opin Y
*.ipin vdd
*.ipin gnd
XM1 Y A net1 gnd sky130_fd_pr__nfet_01v8 L=0.15 W=1 nf=1 ad='int((nf+1)/2) * W/nf * 0.29' as='int((nf+2)/2) * W/nf * 0.29'
+ pd='2*int((nf+1)/2) * (W/nf + 0.29)' ps='2*int((nf+2)/2) * (W/nf + 0.29)' nrd='0.29 / W' nrs='0.29 / W'
+ sa=0 sb=0 sd=0 mult=1 m=1
XM2 net1 B gnd gnd sky130_fd_pr__nfet_01v8 L=0.15 W=1 nf=1 ad='int((nf+1)/2) * W/nf * 0.29' as='int((nf+2)/2) * W/nf * 0.29'
+ pd='2*int((nf+1)/2) * (W/nf + 0.29)' ps='2*int((nf+2)/2) * (W/nf + 0.29)' nrd='0.29 / W' nrs='0.29 / W'
+ sa=0 sb=0 sd=0 mult=1 m=1
XM3 Y A vdd vdd sky130_fd_pr__pfet_01v8 L=0.15 W=2 nf=1 ad='int((nf+1)/2) * W/nf * 0.29' as='int((nf+2)/2) * W/nf * 0.29'
+ pd='2*int((nf+1)/2) * (W/nf + 0.29)' ps='2*int((nf+2)/2) * (W/nf + 0.29)' nrd='0.29 / W' nrs='0.29 / W'
+ sa=0 sb=0 sd=0 mult=1 m=1
XM4 Y B vdd vdd sky130_fd_pr__pfet_01v8 L=0.15 W=2 nf=1 ad='int((nf+1)/2) * W/nf * 0.29' as='int((nf+2)/2) * W/nf * 0.29'
+ pd='2*int((nf+1)/2) * (W/nf + 0.29)' ps='2*int((nf+2)/2) * (W/nf + 0.29)' nrd='0.29 / W' nrs='0.29 / W'
+ sa=0 sb=0 sd=0 mult=1 m=1
.ends

.GLOBAL GND
.GLOBAL VDD
.end
